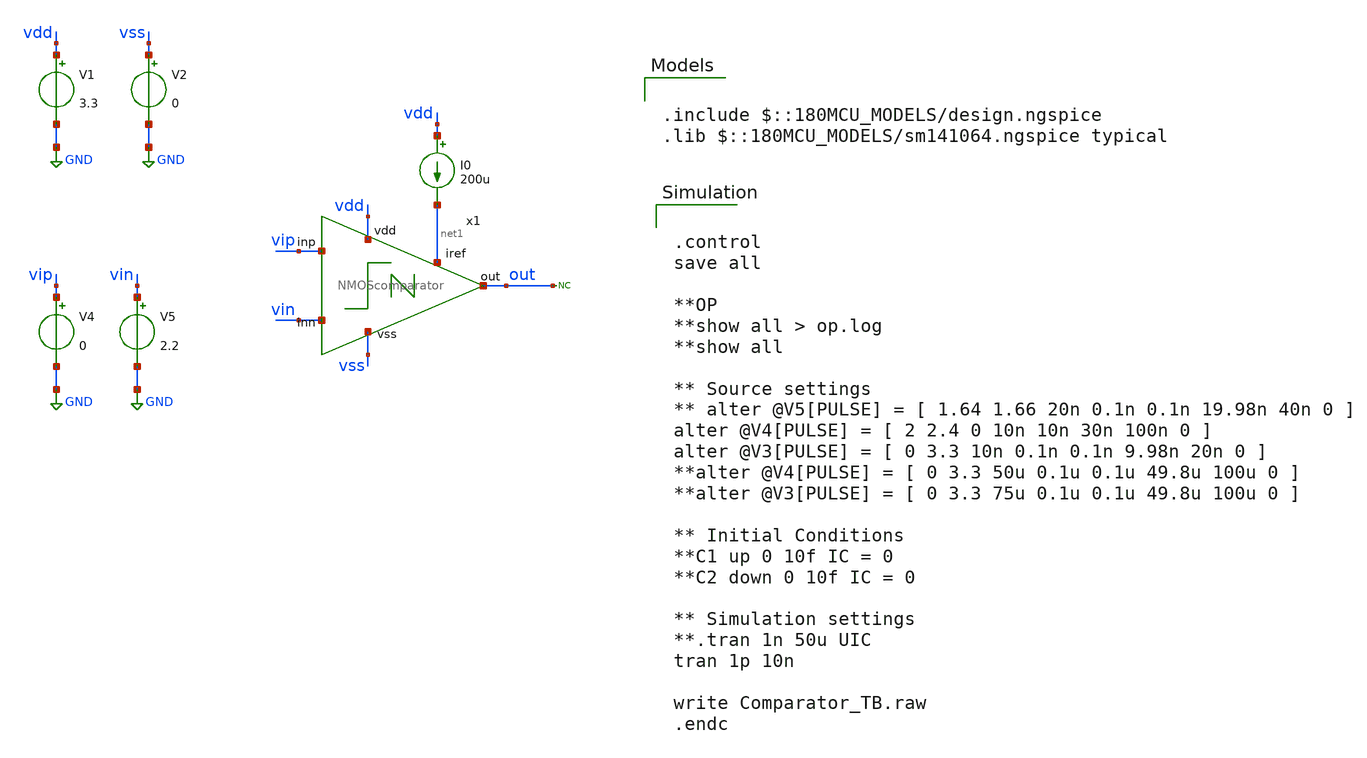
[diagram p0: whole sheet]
** sch_path: designs/libs/qw_core_analog/Comparator_TB.sch
**.subckt Comparator_TB
V1 vdd GND 3.3
V2 vss GND 0
* noconn out
V4 vip GND 0
V5 vin GND 2.2
x1 vdd vip out vin net1 vss NMOScomparator
I0 vdd net1 200u
**** begin user architecture code

.include $::180MCU_MODELS/design.ngspice
.lib $::180MCU_MODELS/sm141064.ngspice typical



.control
save all

**OP
**show all > op.log
**show all

** Source settings
** alter @V5[PULSE] = [ 1.64 1.66 20n 0.1n 0.1n 19.98n 40n 0 ]
alter @V4[PULSE] = [ 2 2.4 0 10n 10n 30n 100n 0 ]
alter @V3[PULSE] = [ 0 3.3 10n 0.1n 0.1n 9.98n 20n 0 ]
**alter @V4[PULSE] = [ 0 3.3 50u 0.1u 0.1u 49.8u 100u 0 ]
**alter @V3[PULSE] = [ 0 3.3 75u 0.1u 0.1u 49.8u 100u 0 ]

** Initial Conditions
**C1 up 0 10f IC = 0
**C2 down 0 10f IC = 0

** Simulation settings
**.tran 1n 50u UIC
tran 1p 10n

write Comparator_TB.raw
.endc


**** end user architecture code
**.ends
.GLOBAL GND
.end
